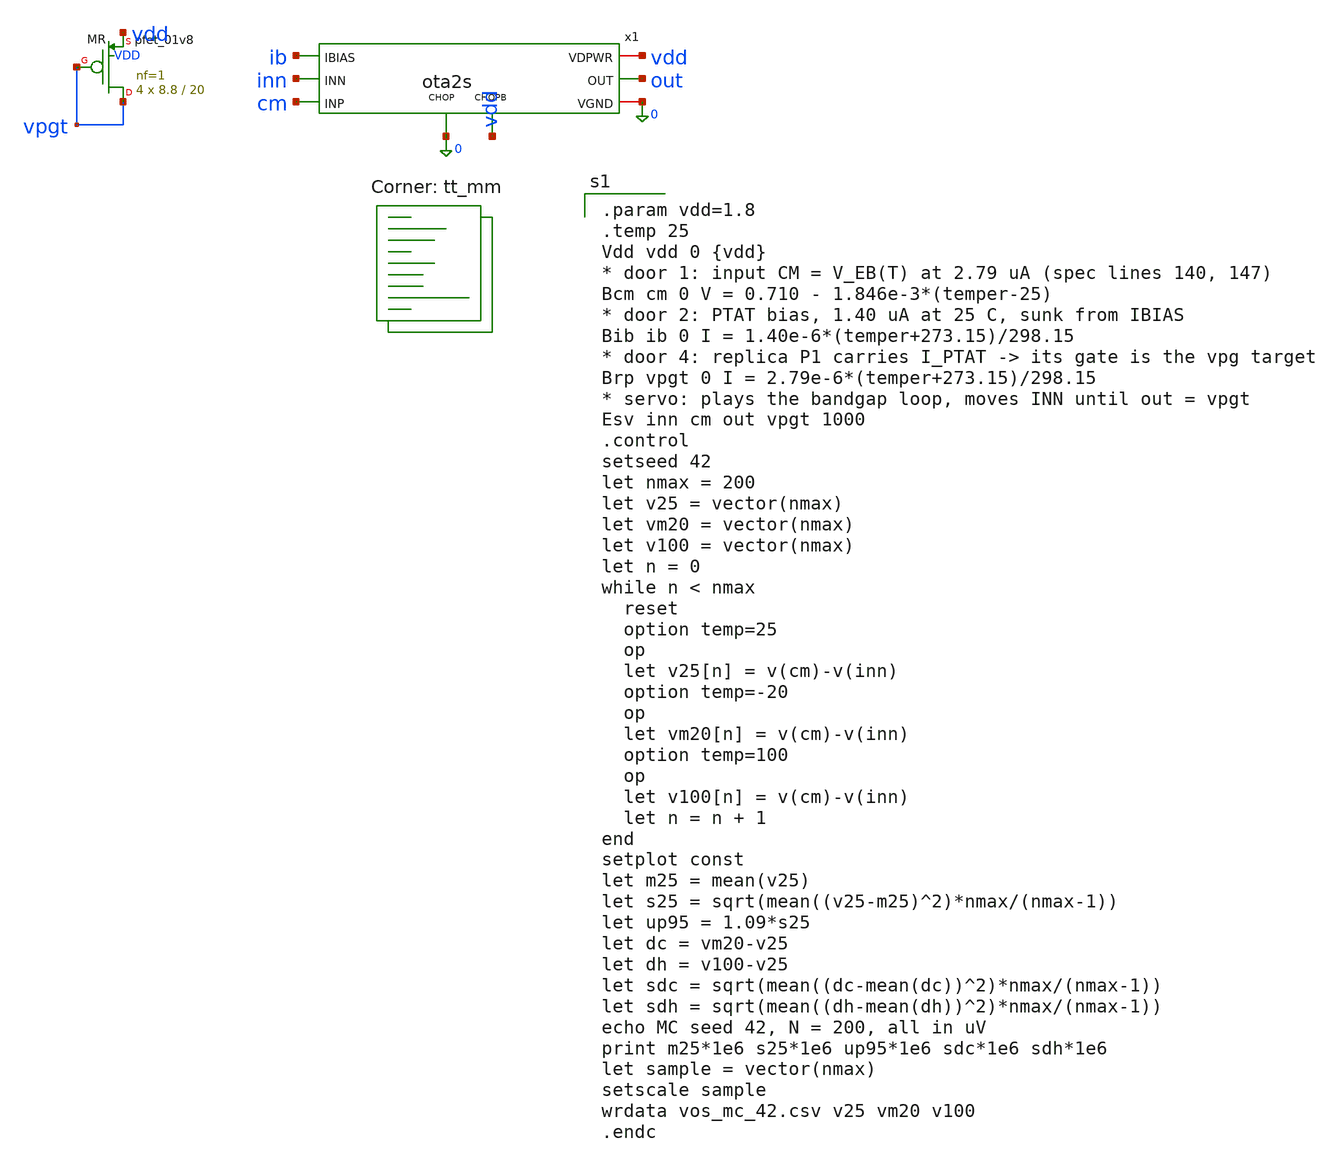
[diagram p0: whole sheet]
** sch_path: xschem/tb_ota2s_mc.sch
**.subckt tb_ota2s_mc
x1 cm inn out vdd 0 ib 0 vdd ota2s
XMR vpgt vpgt vdd VDD sky130_fd_pr__pfet_01v8 L=20 W=8.8 nf=1 ad='int((1 + 1)/2) * 8.8 / 1 * 0.29' as='int((1 + 2)/2) * 8.8 / 1 * 0.29'
+ pd='2*int((1 + 1)/2) * (8.8 / 1 + 0.29)' ps='2*int((1 + 2)/2) * (8.8 / 1 + 0.29)' nrd='0.29 / 8.8 ' nrs='0.29 / 8.8 '
+ sa=0 sb=0 sd=0 mult=4 m=4
**** begin user architecture code
.lib $::SKYWATER_MODELS/sky130.lib.spice tt_mm

.param vdd=1.8
.temp 25
Vdd vdd 0 {vdd}
* door 1: input CM = V_EB(T) at 2.79 uA (spec lines 140, 147)
Bcm cm 0 V = 0.710 - 1.846e-3*(temper-25)
* door 2: PTAT bias, 1.40 uA at 25 C, sunk from IBIAS
Bib ib 0 I = 1.40e-6*(temper+273.15)/298.15
* door 4: replica P1 carries I_PTAT -> its gate is the vpg target
Brp vpgt 0 I = 2.79e-6*(temper+273.15)/298.15
* servo: plays the bandgap loop, moves INN until out = vpgt
Esv inn cm out vpgt 1000
.control
setseed 42
let nmax = 200
let v25 = vector(nmax)
let vm20 = vector(nmax)
let v100 = vector(nmax)
let n = 0
while n < nmax
  reset
  option temp=25
  op
  let v25[n] = v(cm)-v(inn)
  option temp=-20
  op
  let vm20[n] = v(cm)-v(inn)
  option temp=100
  op
  let v100[n] = v(cm)-v(inn)
  let n = n + 1
end
setplot const
let m25 = mean(v25)
let s25 = sqrt(mean((v25-m25)^2)*nmax/(nmax-1))
let up95 = 1.09*s25
let dc = vm20-v25
let dh = v100-v25
let sdc = sqrt(mean((dc-mean(dc))^2)*nmax/(nmax-1))
let sdh = sqrt(mean((dh-mean(dh))^2)*nmax/(nmax-1))
echo MC seed 42, N = 200, all in uV
print m25*1e6 s25*1e6 up95*1e6 sdc*1e6 sdh*1e6
let sample = vector(nmax)
setscale sample
wrdata vos_mc_42.csv v25 vm20 v100
.endc

**** end user architecture code
**.ends

* expanding   symbol:  ota2s.sym # of pins=8
** sym_path: xschem/ota2s.sym
** sch_path: xschem/ota2s.sch
.subckt ota2s INP INN OUT VDPWR VGND IBIAS CHOP CHOPB
*.ipin INN
*.ipin INP
*.ipin IBIAS
*.opin OUT
*.iopin VDPWR
*.iopin VGND
*.ipin CHOPB
*.ipin CHOP
XMREF IBIAS IBIAS VDPWR VDPWR sky130_fd_pr__pfet_01v8 L=4 W=20 nf=1 ad='int((1 + 1)/2) * 20 / 1 * 0.29'
+ as='int((1 + 2)/2) * 20 / 1 * 0.29' pd='2*int((1 + 1)/2) * (20 / 1 + 0.29)' ps='2*int((1 + 2)/2) * (20 / 1 + 0.29)'
+ nrd='0.29 / 20 ' nrs='0.29 / 20 ' sa=0 sb=0 sd=0 mult=1 m=1
XMTAIL tail IBIAS VDPWR VDPWR sky130_fd_pr__pfet_01v8 L=4 W=20 nf=1 ad='int((1 + 1)/2) * 20 / 1 * 0.29'
+ as='int((1 + 2)/2) * 20 / 1 * 0.29' pd='2*int((1 + 1)/2) * (20 / 1 + 0.29)' ps='2*int((1 + 2)/2) * (20 / 1 + 0.29)'
+ nrd='0.29 / 20 ' nrs='0.29 / 20 ' sa=0 sb=0 sd=0 mult=2 m=2
XMP1 d1 INN tail VDPWR sky130_fd_pr__pfet_01v8_lvt L=6 W=25 nf=1 ad='int((1 + 1)/2) * 25 / 1 * 0.29'
+ as='int((1 + 2)/2) * 25 / 1 * 0.29' pd='2*int((1 + 1)/2) * (25 / 1 + 0.29)' ps='2*int((1 + 2)/2) * (25 / 1 + 0.29)'
+ nrd='0.29 / 25 ' nrs='0.29 / 25 ' sa=0 sb=0 sd=0 mult=24 m=24
XMP2 x1 INP tail VDPWR sky130_fd_pr__pfet_01v8_lvt L=6 W=25 nf=1 ad='int((1 + 1)/2) * 25 / 1 * 0.29'
+ as='int((1 + 2)/2) * 25 / 1 * 0.29' pd='2*int((1 + 1)/2) * (25 / 1 + 0.29)' ps='2*int((1 + 2)/2) * (25 / 1 + 0.29)'
+ nrd='0.29 / 25 ' nrs='0.29 / 25 ' sa=0 sb=0 sd=0 mult=24 m=24
XMN1 d1 g12 VGND VGND sky130_fd_pr__nfet_01v8 L=20 W=6 nf=1 ad='int((1 + 1)/2) * 6 / 1 * 0.29' as='int((1 + 2)/2) * 6 / 1 * 0.29'
+ pd='2*int((1 + 1)/2) * (6 / 1 + 0.29)' ps='2*int((1 + 2)/2) * (6 / 1 + 0.29)' nrd='0.29 / 6 ' nrs='0.29 / 6 '
+ sa=0 sb=0 sd=0 mult=2 m=2
XMN2 x1 g12 VGND VGND sky130_fd_pr__nfet_01v8 L=20 W=6 nf=1 ad='int((1 + 1)/2) * 6 / 1 * 0.29' as='int((1 + 2)/2) * 6 / 1 * 0.29'
+ pd='2*int((1 + 1)/2) * (6 / 1 + 0.29)' ps='2*int((1 + 2)/2) * (6 / 1 + 0.29)' nrd='0.29 / 6 ' nrs='0.29 / 6 '
+ sa=0 sb=0 sd=0 mult=2 m=2
XMP3 OUT IBIAS VDPWR VDPWR sky130_fd_pr__pfet_01v8 L=4 W=20 nf=1 ad='int((1 + 1)/2) * 20 / 1 * 0.29'
+ as='int((1 + 2)/2) * 20 / 1 * 0.29' pd='2*int((1 + 1)/2) * (20 / 1 + 0.29)' ps='2*int((1 + 2)/2) * (20 / 1 + 0.29)'
+ nrd='0.29 / 20 ' nrs='0.29 / 20 ' sa=0 sb=0 sd=0 mult=6 m=6
XMN3 OUT g3 VGND VGND sky130_fd_pr__nfet_01v8 L=1 W=7 nf=1 ad='int((1 + 1)/2) * 7 / 1 * 0.29' as='int((1 + 2)/2) * 7 / 1 * 0.29'
+ pd='2*int((1 + 1)/2) * (7 / 1 + 0.29)' ps='2*int((1 + 2)/2) * (7 / 1 + 0.29)' nrd='0.29 / 7 ' nrs='0.29 / 7 '
+ sa=0 sb=0 sd=0 mult=1 m=1
XRZ1 net1 g3 VGND sky130_fd_pr__res_high_po_1p41 L=20 mult=1 m=1
XRZ2 net2 net1 VGND sky130_fd_pr__res_high_po_1p41 L=20 mult=1 m=1
XRZ3 net3 net2 VGND sky130_fd_pr__res_high_po_1p41 L=20 mult=1 m=1
XRZ4 net4 net3 VGND sky130_fd_pr__res_high_po_1p41 L=20 mult=1 m=1
XRZ5 net5 net4 VGND sky130_fd_pr__res_high_po_1p41 L=20 mult=1 m=1
XRZ6 cz net5 VGND sky130_fd_pr__res_high_po_1p41 L=20 mult=1 m=1
XCC cz OUT sky130_fd_pr__cap_mim_m3_1 W=25 L=25 MF=8 m=8
XDP tail VDPWR tail VDPWR sky130_fd_pr__pfet_01v8_lvt L=6 W=25 nf=1 ad='int((1 + 1)/2) * 25 / 1 * 0.29'
+ as='int((1 + 2)/2) * 25 / 1 * 0.29' pd='2*int((1 + 1)/2) * (25 / 1 + 0.29)' ps='2*int((1 + 2)/2) * (25 / 1 + 0.29)'
+ nrd='0.29 / 25 ' nrs='0.29 / 25 ' sa=0 sb=0 sd=0 mult=8 m=8
XDNA d1 VGND VGND VGND sky130_fd_pr__nfet_01v8 L=20 W=6 nf=1 ad='int((1 + 1)/2) * 6 / 1 * 0.29' as='int((1 + 2)/2) * 6 / 1 * 0.29'
+ pd='2*int((1 + 1)/2) * (6 / 1 + 0.29)' ps='2*int((1 + 2)/2) * (6 / 1 + 0.29)' nrd='0.29 / 6 ' nrs='0.29 / 6 '
+ sa=0 sb=0 sd=0 mult=2 m=2
XDNB x1 VGND VGND VGND sky130_fd_pr__nfet_01v8 L=20 W=6 nf=1 ad='int((1 + 1)/2) * 6 / 1 * 0.29' as='int((1 + 2)/2) * 6 / 1 * 0.29'
+ pd='2*int((1 + 1)/2) * (6 / 1 + 0.29)' ps='2*int((1 + 2)/2) * (6 / 1 + 0.29)' nrd='0.29 / 6 ' nrs='0.29 / 6 '
+ sa=0 sb=0 sd=0 mult=2 m=2
XDB VDPWR VDPWR VDPWR VDPWR sky130_fd_pr__pfet_01v8 L=4 W=20 nf=1 ad='int((1 + 1)/2) * 20 / 1 * 0.29'
+ as='int((1 + 2)/2) * 20 / 1 * 0.29' pd='2*int((1 + 1)/2) * (20 / 1 + 0.29)' ps='2*int((1 + 2)/2) * (20 / 1 + 0.29)'
+ nrd='0.29 / 20 ' nrs='0.29 / 20 ' sa=0 sb=0 sd=0 mult=2 m=2
XRD1 VGND VGND VGND sky130_fd_pr__res_high_po_1p41 L=20 mult=1 m=1
XRD2 VGND VGND VGND sky130_fd_pr__res_high_po_1p41 L=20 mult=1 m=1
XSD1 d1 CHOPB g12 VGND sky130_fd_pr__nfet_01v8 L=0.5 W=6 nf=1 ad='int((1 + 1)/2) * 6 / 1 * 0.29' as='int((1 + 2)/2) * 6 / 1 * 0.29'
+ pd='2*int((1 + 1)/2) * (6 / 1 + 0.29)' ps='2*int((1 + 2)/2) * (6 / 1 + 0.29)' nrd='0.29 / 6 ' nrs='0.29 / 6 '
+ sa=0 sb=0 sd=0 mult=1 m=1
XSD2 x1 CHOP g12 VGND sky130_fd_pr__nfet_01v8 L=0.5 W=6 nf=1 ad='int((1 + 1)/2) * 6 / 1 * 0.29' as='int((1 + 2)/2) * 6 / 1 * 0.29'
+ pd='2*int((1 + 1)/2) * (6 / 1 + 0.29)' ps='2*int((1 + 2)/2) * (6 / 1 + 0.29)' nrd='0.29 / 6 ' nrs='0.29 / 6 '
+ sa=0 sb=0 sd=0 mult=1 m=1
XSG2 g3 CHOP d1 VGND sky130_fd_pr__nfet_01v8 L=0.5 W=6 nf=1 ad='int((1 + 1)/2) * 6 / 1 * 0.29' as='int((1 + 2)/2) * 6 / 1 * 0.29'
+ pd='2*int((1 + 1)/2) * (6 / 1 + 0.29)' ps='2*int((1 + 2)/2) * (6 / 1 + 0.29)' nrd='0.29 / 6 ' nrs='0.29 / 6 '
+ sa=0 sb=0 sd=0 mult=1 m=1
XSG1 x1 CHOPB g3 VGND sky130_fd_pr__nfet_01v8 L=0.5 W=6 nf=1 ad='int((1 + 1)/2) * 6 / 1 * 0.29' as='int((1 + 2)/2) * 6 / 1 * 0.29'
+ pd='2*int((1 + 1)/2) * (6 / 1 + 0.29)' ps='2*int((1 + 2)/2) * (6 / 1 + 0.29)' nrd='0.29 / 6 ' nrs='0.29 / 6 '
+ sa=0 sb=0 sd=0 mult=1 m=1
.ends

.end
